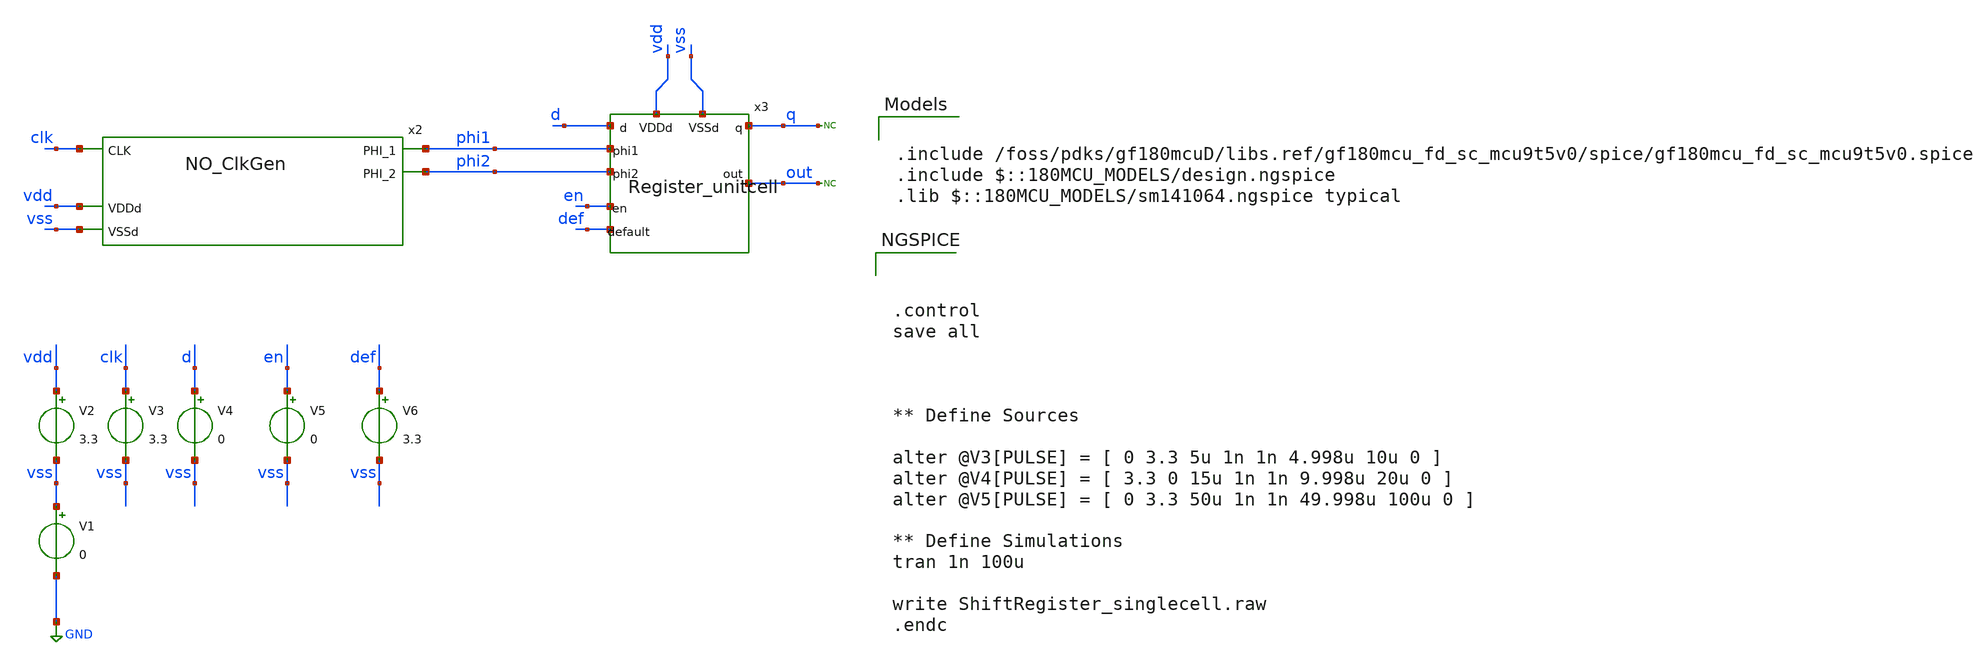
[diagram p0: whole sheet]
** sch_path: designs/libs/qw_core_analog/ShiftRegister_singlecell/ShiftRegister_singlecell.sch
**.subckt ShiftRegister_singlecell
V1 vss GND 0
V2 vdd vss 3.3
x2 phi2 clk phi1 vdd vss NO_ClkGen
V3 clk vss 3.3
V4 d vss 0
* noconn out
V5 en vss 0
V6 def vss 3.3
* noconn q
x3 q d phi1 phi2 vdd vss out en def Register_unitcell
**** begin user architecture code

.include /foss/pdks/gf180mcuD/libs.ref/gf180mcu_fd_sc_mcu9t5v0/spice/gf180mcu_fd_sc_mcu9t5v0.spice
.include $::180MCU_MODELS/design.ngspice
.lib $::180MCU_MODELS/sm141064.ngspice typical




.control
save all



** Define Sources

alter @V3[PULSE] = [ 0 3.3 5u 1n 1n 4.998u 10u 0 ]
alter @V4[PULSE] = [ 3.3 0 15u 1n 1n 9.998u 20u 0 ]
alter @V5[PULSE] = [ 0 3.3 50u 1n 1n 49.998u 100u 0 ]

** Define Simulations
tran 1n 100u

write ShiftRegister_singlecell.raw
.endc


**** end user architecture code
**.ends

* expanding   symbol:  switch_matrix_gf180mcu_9t5v0-main/NO_ClkGen/NO_ClkGen.sym # of pins=5
** sym_path: designs/switch_matrix_gf180mcu_9t5v0-main/NO_ClkGen/NO_ClkGen.sym
** sch_path: designs/switch_matrix_gf180mcu_9t5v0-main/NO_ClkGen/NO_ClkGen.sch
.subckt NO_ClkGen PHI_2 CLK PHI_1 VDDd VSSd
*.ipin CLK
*.opin PHI_2
*.iopin VDDd
*.iopin VSSd
*.opin PHI_1
* noconn VDDd
* noconn VSSd
x21 CLK VSSd VDDd VSSd VDDd CLKB gf180mcu_fd_sc_mcu9t5v0__inv_1
x22 CLKB OUT_bot_d VSSd VDDd VSSd VDDd OUT_top gf180mcu_fd_sc_mcu9t5v0__nand2_1
x1 OUT_top_d CLKbuf VSSd VDDd VSSd VDDd OUT_bot gf180mcu_fd_sc_mcu9t5v0__nand2_1
x2 CLKB VSSd VDDd VSSd VDDd CLKbuf gf180mcu_fd_sc_mcu9t5v0__inv_1
x6 OUT_bot VSSd VDDd VSSd VDDd PHI_1 gf180mcu_fd_sc_mcu9t5v0__inv_1
x7 PHI_1 VSSd VDDd VSSd VDDd net2 gf180mcu_fd_sc_mcu9t5v0__inv_1
x8 net2 VSSd VDDd VSSd VDDd net8 gf180mcu_fd_sc_mcu9t5v0__inv_1
x9 net8 VSSd VDDd VSSd VDDd net6 gf180mcu_fd_sc_mcu9t5v0__inv_1
x10 net6 VSSd VDDd VSSd VDDd net4 gf180mcu_fd_sc_mcu9t5v0__inv_1
x12 net4 VSSd VDDd VSSd VDDd net12 gf180mcu_fd_sc_mcu9t5v0__inv_1
x15 net12 VSSd VDDd VSSd VDDd net10 gf180mcu_fd_sc_mcu9t5v0__inv_1
x16 net10 VSSd VDDd VSSd VDDd OUT_bot_d gf180mcu_fd_sc_mcu9t5v0__inv_1
x3 OUT_top VSSd VDDd VSSd VDDd PHI_2 gf180mcu_fd_sc_mcu9t5v0__inv_1
x4 PHI_2 VSSd VDDd VSSd VDDd net1 gf180mcu_fd_sc_mcu9t5v0__inv_1
x5 net1 VSSd VDDd VSSd VDDd net7 gf180mcu_fd_sc_mcu9t5v0__inv_1
x11 net7 VSSd VDDd VSSd VDDd net5 gf180mcu_fd_sc_mcu9t5v0__inv_1
x13 net5 VSSd VDDd VSSd VDDd net3 gf180mcu_fd_sc_mcu9t5v0__inv_1
x14 net3 VSSd VDDd VSSd VDDd net11 gf180mcu_fd_sc_mcu9t5v0__inv_1
x17 net11 VSSd VDDd VSSd VDDd net9 gf180mcu_fd_sc_mcu9t5v0__inv_1
x18 net9 VSSd VDDd VSSd VDDd OUT_top_d gf180mcu_fd_sc_mcu9t5v0__inv_1
.ends


* expanding   symbol:  libs/qw_core_analog/Register_unitcell/Register_unitcell.sym # of pins=9
** sym_path: designs/libs/qw_core_analog/Register_unitcell/Register_unitcell.sym
** sch_path: designs/libs/qw_core_analog/Register_unitcell/Register_unitcell.sch
.subckt Register_unitcell q d phi1 phi2 VDDd VSSd out en default
*.iopin phi1
*.iopin phi2
*.iopin d
*.iopin q
*.iopin en
*.iopin default
*.iopin out
*.iopin VDDd
*.iopin VSSd
x4 en VSSd VDDd VSSd VDDd enbar gf180mcu_fd_sc_mcu9t5v0__inv_1
* noconn VDDd
* noconn VSSd
x1 d q phi1 phi2 DFF_2phase_1
x2 q en VSSd VDDd VSSd VDDd or1 gf180mcu_fd_sc_mcu9t5v0__and2_1
x10 or2 or1 VSSd VDDd VSSd VDDd out gf180mcu_fd_sc_mcu9t5v0__or2_1
x3 enbar default VSSd VDDd VSSd VDDd or2 gf180mcu_fd_sc_mcu9t5v0__and2_1
.ends


* expanding   symbol:  libs/qw_core_analog/DFF_2phase_1/DFF_2phase_1.sym # of pins=4
** sym_path: designs/switch_matrix_gf180mcu_9t5v0-main/designs/libs/core_swmatrix/DFF_2phase_1.sym
** sch_path: designs/switch_matrix_gf180mcu_9t5v0-main/designs/libs/core_swmatrix/DFF_2phase_1.sch
.subckt DFF_2phase_1 D Q PHI_1 PHI_2
*.ipin D
*.ipin PHI_1
*.ipin PHI_2
*.opin Q
xmain D PHI_1 out_m VDDd VDDd VSSd VSSd gf180mcu_fd_sc_mcu9t5v0__latq_1
xsecondary out_m PHI_2 Q VDDd VDDd VSSd VSSd gf180mcu_fd_sc_mcu9t5v0__latq_1
.ends

.GLOBAL GND
.end
